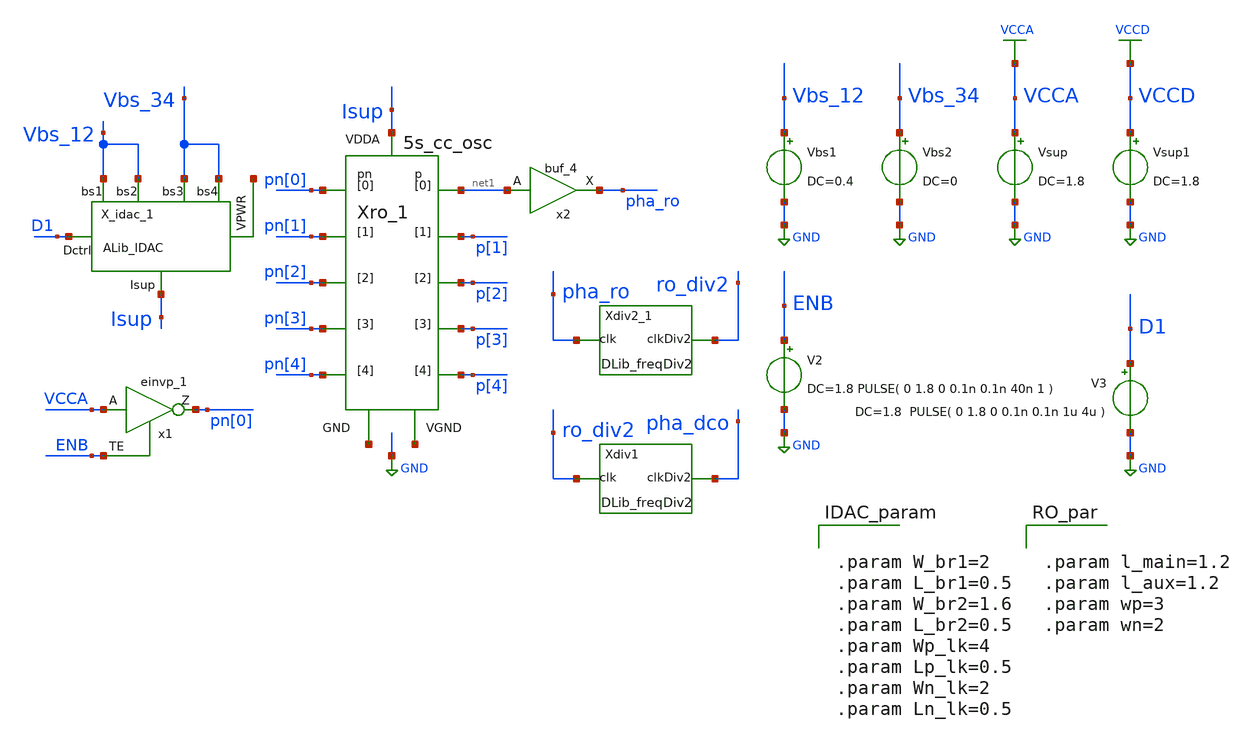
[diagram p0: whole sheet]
** sch_path: xschem/tb/IDAC_tb.sch

.include $::SKYWATER_STDCELLS/sky130_fd_sc_hd.spice
.lib $::SKYWATER_MODELS/sky130.lib.spice tt

**.subckt IDAC_tb
Vsup VCCA GND DC=1.8
Vbs1 Vbs_12 GND DC=0.4
x1 VCCA ENB VGND VNB VPB VPWR pn[0] sky130_fd_sc_hd__einvp_1
V2 ENB GND DC=1.8 PULSE( 0 1.8 0 0.1n 0.1n 40n 1 )
V3 D1 GND DC=1.8 PULSE( 0 1.8 0 0.1n 0.1n 1u 4u )
X_idac_1 D1 Vbs_12 Vbs_12 Vbs_34 Vbs_34 net2 Isup ALib_IDAC W_br1="W_br1" L_br1="L_br1"
+ W_br2="W_br2" L_br2="L_br2" Wp_lk="Wp_lk" Lp_lk="Lp_lk" Wn_lk="Wn_lk" Ln_lk="Wn_lk"
Vbs2 Vbs_34 GND DC=0
x2 net1 GND GND VCCD VCCD pha_ro sky130_fd_sc_hd__buf_4
Vsup1 VCCD GND DC=1.8
Xdiv2_1 pha_ro GND GND VCCD VCCD ro_div2 DLib_freqDiv2
Xro_1 net3 Isup net1 p[1] p[2] p[3] p[4] pn[0] pn[1] pn[2] pn[3] pn[4] net4 5s_cc_osc
Xdiv1 ro_div2 GND GND VCCD VCCD pha_dco DLib_freqDiv2
**** begin user architecture code


.param W_br1=2
.param L_br1=0.5
.param W_br2=1.6
.param L_br2=0.5
.param Wp_lk=4
.param Lp_lk=0.5
.param Wn_lk=2
.param Ln_lk=0.5

**** end user architecture code
**.ends
.GLOBAL GND
.GLOBAL VCCA
.GLOBAL VCCD
**** begin user architecture code


.save all
.tran 1n 50u start=0 $  sweep vin 0 1.0 0.1
.measure tran prd1 trig v(pha_dco) val=0.8 rise=10 targ v(pha_dco) val=0.8 rise=30
.measure tran freq_d param='20/prd1'
** options for finesim simulator
.option finesim_fsdb_version=5.6
.option finesim_output=fsdb
.option finesim_mode=ALib*:spicead:p:subckt
.option finesim_mode=DLib*:promd:subckt
.option finesim_mode=promd




.param l_main=1.2
.param l_aux=1.2
.param wp=3
.param wn=2

**** end user architecture code
.end
